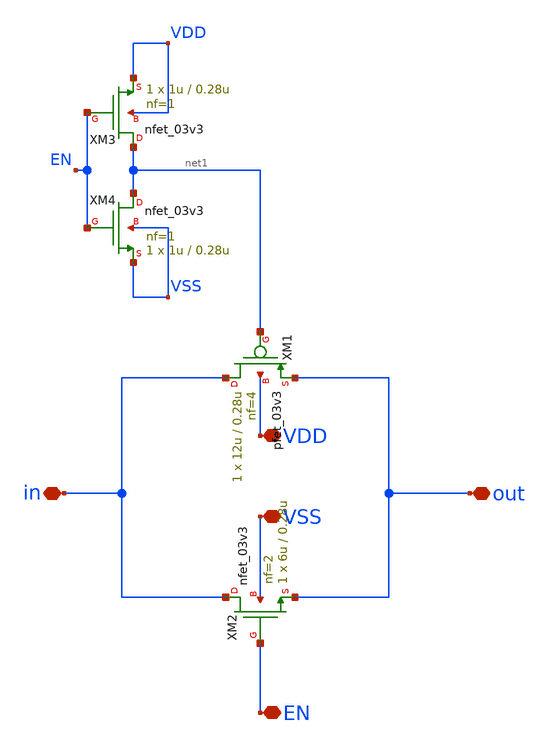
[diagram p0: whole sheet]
** sch_path: designs/digital/schematic/transmission_gate_high_impedance.sch
**.subckt transmission_gate_high_impedance VDD VSS in out EN
*.iopin VDD
*.iopin VSS
*.iopin in
*.iopin out
*.iopin EN
XM1 in net1 out VDD pfet_03v3 L=0.28u W=12u nf=4 ad='int((nf+1)/2) * W/nf * 0.18u' as='int((nf+2)/2) * W/nf * 0.18u'
+ pd='2*int((nf+1)/2) * (W/nf + 0.18u)' ps='2*int((nf+2)/2) * (W/nf + 0.18u)' nrd='0.18u / W' nrs='0.18u / W'
+ sa=0 sb=0 sd=0 m=1
XM2 in EN out VSS nfet_03v3 L=0.28u W=6u nf=2 ad='int((nf+1)/2) * W/nf * 0.18u' as='int((nf+2)/2) * W/nf * 0.18u'
+ pd='2*int((nf+1)/2) * (W/nf + 0.18u)' ps='2*int((nf+2)/2) * (W/nf + 0.18u)' nrd='0.18u / W' nrs='0.18u / W'
+ sa=0 sb=0 sd=0 m=1
XM3 net1 EN VDD VDD nfet_03v3 L=0.28u W=1u nf=1 ad='int((nf+1)/2) * W/nf * 0.18u' as='int((nf+2)/2) * W/nf * 0.18u'
+ pd='2*int((nf+1)/2) * (W/nf + 0.18u)' ps='2*int((nf+2)/2) * (W/nf + 0.18u)' nrd='0.18u / W' nrs='0.18u / W'
+ sa=0 sb=0 sd=0 m=1
XM4 net1 EN VSS VSS nfet_03v3 L=0.28u W=1u nf=1 ad='int((nf+1)/2) * W/nf * 0.18u' as='int((nf+2)/2) * W/nf * 0.18u'
+ pd='2*int((nf+1)/2) * (W/nf + 0.18u)' ps='2*int((nf+2)/2) * (W/nf + 0.18u)' nrd='0.18u / W' nrs='0.18u / W'
+ sa=0 sb=0 sd=0 m=1
**.ends
.end
